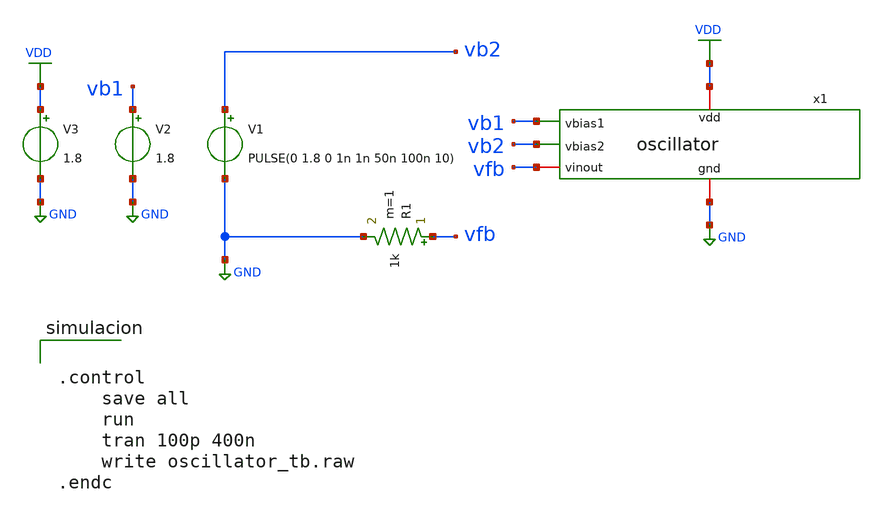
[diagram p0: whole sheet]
** sch_path: oscillator/oscillator_tb.sch
**.subckt oscillator_tb
x1 VDD vb1 vfb vb2 GND oscillator
V1 vb2 GND PULSE(0 1.8 0 1n 1n 50n 100n 10)
.save i(v1)
V2 vb1 GND 1.8
.save i(v2)
V3 VDD GND 1.8
.save i(v3)
R1 vfb GND 1k m=1
**** begin user architecture code

** opencircuitdesign pdks install
.lib $::SKYWATER_MODELS/sky130.lib.spice tt




.control
	save all
	run
	tran 100p 400n
	write oscillator_tb.raw
.endc


**** end user architecture code
**.ends
.GLOBAL VDD
.GLOBAL GND
.end
